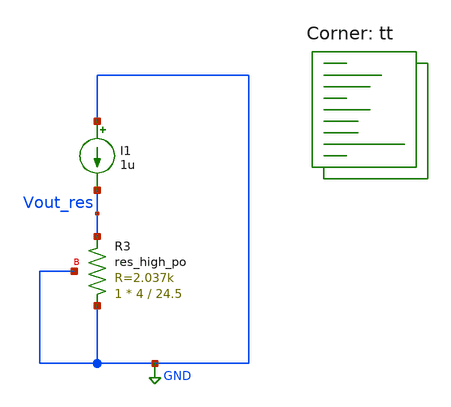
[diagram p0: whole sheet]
** sch_path: design/misc/testing/res.sch
**.subckt res
I1 GND Vout_res 1u
XR3 GND Vout_res GND sky130_fd_pr__res_high_po W=4 L=24.5 mult=1 m=1
**** begin user architecture code
.lib $::SKYWATER_MODELS/sky130.lib.spice tt


.param temp=27

.dc temp -40 125 1


.save all
.control
run
plot Vout_res
plot deriv(Vout_res)
.endc



**** end user architecture code
**.ends
.GLOBAL GND
.end
